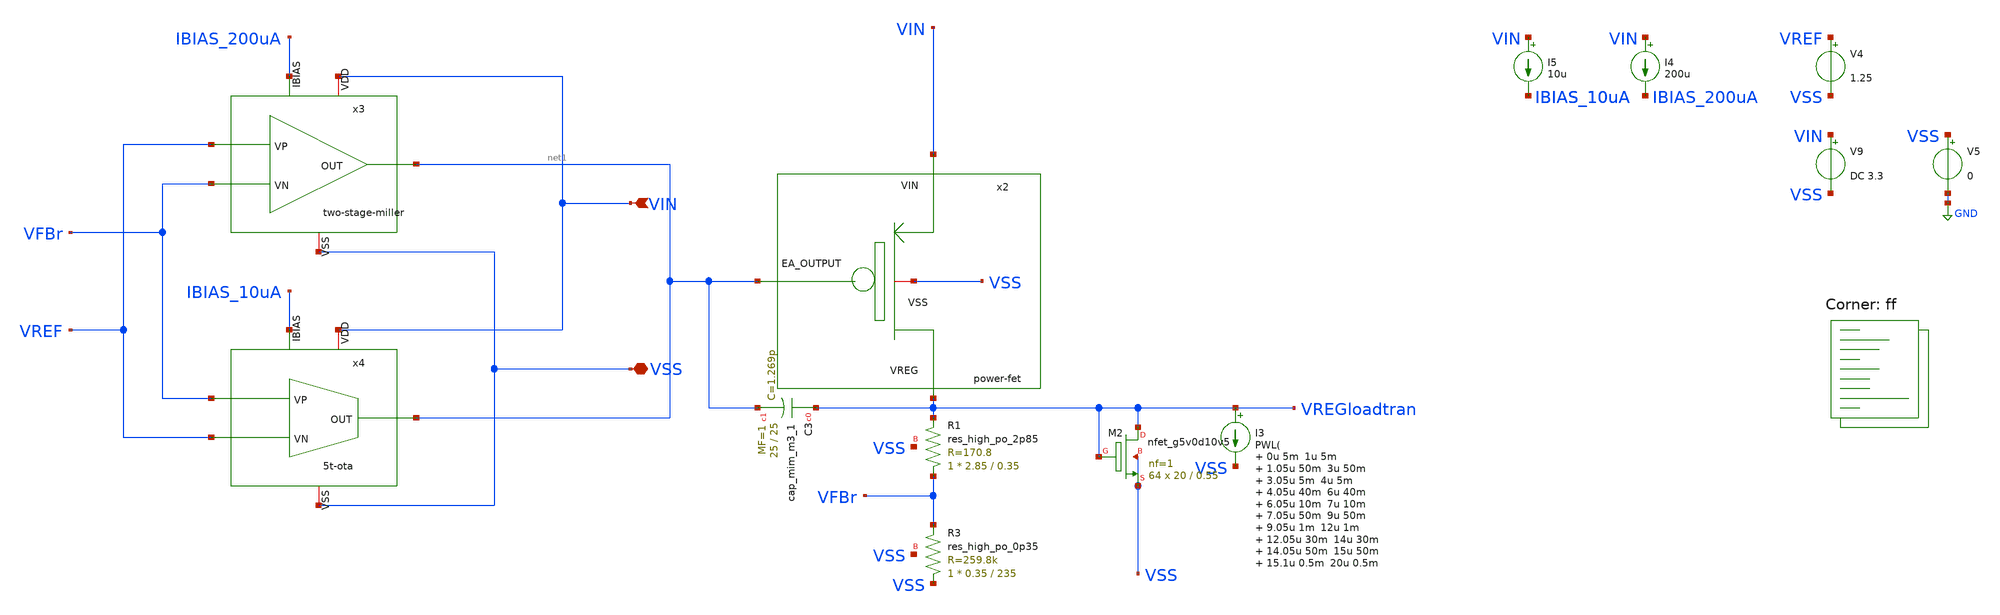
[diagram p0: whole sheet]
** sch_path: xschem/ldo-core/tb_tran_standalone.sch
**.subckt tb_tran_standalone VIN VSS
*.ipin VIN
*.iopin VSS
x2 VIN VSS net1 VREGloadtran power-fet
XR3 VSS VFBr VSS sky130_fd_pr__res_high_po_0p35 L=235 mult=1 m=1
XR1 VFBr VREGloadtran VSS sky130_fd_pr__res_high_po_2p85 L=0.35 mult=1 m=1
x3 VIN net1 VREF VFBr IBIAS_200uA VSS two-stage-miller
x4 VIN net1 IBIAS_10uA VREF VFBr VSS 5t-ota
I4 VIN IBIAS_200uA 200u
I3 VREGloadtran VSS PWL( 0u 5m 1u 5m 1.05u 50m 3u 50m 3.05u 5m 4u 5m 4.05u 40m 6u 40m 6.05u 10m 7u
+ 10m 7.05u 50m 9u 50m 9.05u 1m 12u 1m 12.05u 30m 14u 30m 14.05u 50m 15u 50m 15.1u 0.5m 20u 0.5m
)
V4 VREF VSS 1.25
V5 VSS GND 0
V9 VIN VSS DC 3.3
I5 VIN IBIAS_10uA 10u
XM2 VREGloadtran VREGloadtran VSS VSS sky130_fd_pr__nfet_g5v0d10v5 L=0.55 W=20 nf=1 ad='int((nf+1)/2) * W/nf * 0.29'
+ as='int((nf+2)/2) * W/nf * 0.29' pd='2*int((nf+1)/2) * (W/nf + 0.29)' ps='2*int((nf+2)/2) * (W/nf + 0.29)'
+ nrd='0.29 / W' nrs='0.29 / W' sa=0 sb=0 sd=0 mult=64 m=64
XC3 VREGloadtran net1 sky130_fd_pr__cap_mim_m3_1 W=25 L=25 MF=1 m=1
**** begin user architecture code



.temp 27
.control

tran 0.1u 30u

* Nominal output voltage (from regulation region)
let Vout_nom = 1.25
let Vout_95  = 0.95*Vout_nom

* Find Vin where Vout crosses 95%
meas dc Vin_do find v(vin) when v(vreg)=Vout_95

* Measure Vout at that Vin (for completeness)
meas dc Vout_do find v(vreg) when v(vreg)=Vout_95

* Compute dropout voltage
let Vdo = Vin_do - Vout_do

* Compute overshoot, undershoot and peak-to-peak voltage
meas tran Vout_max MAX v(VREGloadtran)
meas tran Vout_min MIN v(VREGloadtran)
let vpp = Vout_max - Vout_min

print Vin_do Vout_do Vdo
print Vout_max Vout_min Vpp
plot VREGloadtran
plot VREGloadtran2
plot VREG
plot VIN
plot I(Vmeas)

.endc


.lib $::SKYWATER_MODELS/sky130.lib.spice ff
**** end user architecture code
**.ends
.GLOBAL GND
.end
